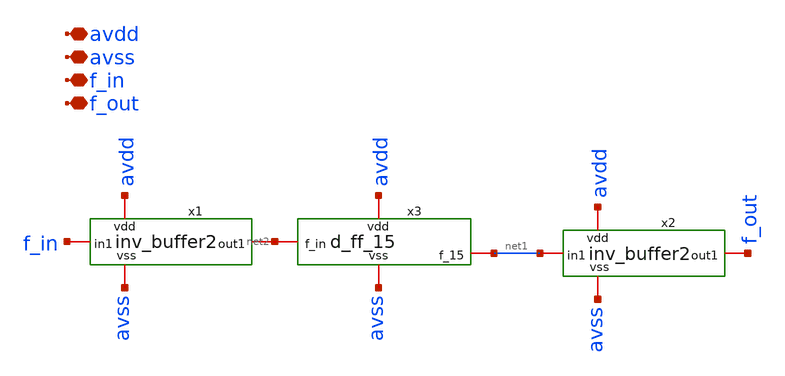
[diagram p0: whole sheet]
** sch_path: xschem/f_div.sch
**.subckt f_div avdd avss f_in f_out
*.iopin avdd
*.iopin avss
*.iopin f_in
*.iopin f_out
x1 avdd avss net2 f_in inv_buffer2
x2 avdd avss f_out net1 inv_buffer2
x3 avdd avss net2 net1 d_ff_15
**.ends

* expanding   symbol:  inv_buffer2.sym # of pins=4
** sym_path: xschem/inv_buffer2.sym
** sch_path: xschem/inv_buffer2.sch
.subckt inv_buffer2 vdd vss out1 in1
*.iopin in1
*.iopin out1
*.iopin vdd
*.iopin vss
XM4 out1 net1 vss vss sky130_fd_pr__nfet_01v8 L=0.15 W=2.8 nf=4 ad='int((nf+1)/2) * W/nf * 0.29' as='int((nf+2)/2) * W/nf * 0.29'
+ pd='2*int((nf+1)/2) * (W/nf + 0.29)' ps='2*int((nf+2)/2) * (W/nf + 0.29)' nrd='0.29 / W' nrs='0.29 / W'
+ sa=0 sb=0 sd=0 mult=1 m=1
XM1 out1 net1 vdd vdd sky130_fd_pr__pfet_01v8 L=0.15 W=5.6 nf=8 ad='int((nf+1)/2) * W/nf * 0.29' as='int((nf+2)/2) * W/nf * 0.29'
+ pd='2*int((nf+1)/2) * (W/nf + 0.29)' ps='2*int((nf+2)/2) * (W/nf + 0.29)' nrd='0.29 / W' nrs='0.29 / W'
+ sa=0 sb=0 sd=0 mult=1 m=1
XM5 vdd vdd vdd vdd sky130_fd_pr__pfet_01v8 L=0.15 W=1.4 nf=2 ad='int((nf+1)/2) * W/nf * 0.29' as='int((nf+2)/2) * W/nf * 0.29'
+ pd='2*int((nf+1)/2) * (W/nf + 0.29)' ps='2*int((nf+2)/2) * (W/nf + 0.29)' nrd='0.29 / W' nrs='0.29 / W'
+ sa=0 sb=0 sd=0 mult=1 m=1
XM6 vss vss vss vss sky130_fd_pr__nfet_01v8 L=0.15 W=1.4 nf=2 ad='int((nf+1)/2) * W/nf * 0.29' as='int((nf+2)/2) * W/nf * 0.29'
+ pd='2*int((nf+1)/2) * (W/nf + 0.29)' ps='2*int((nf+2)/2) * (W/nf + 0.29)' nrd='0.29 / W' nrs='0.29 / W'
+ sa=0 sb=0 sd=0 mult=1 m=1
x1 vdd in1 net1 vss inv_simple1
.ends


* expanding   symbol:  d_ff_15.sym # of pins=4
** sym_path: xschem/d_ff_15.sym
** sch_path: xschem/d_ff_15.sch
.subckt d_ff_15 vdd vss f_in f_15
*.iopin vdd
*.iopin vss
*.iopin f_in
*.iopin f_15
x1 f_in net3 vss vss vdd vdd f_5 q_1 sky130_fd_sc_hd__dfxbp_1
x5 net2 net1 vss vss vdd vdd net3 sky130_fd_sc_hd__nand2_1
x2 f_in f_5 vss vss vdd vdd net1 q_2 sky130_fd_sc_hd__dfxbp_1
x3 f_in net1 vss vss vdd vdd net2 q_3 sky130_fd_sc_hd__dfxbp_1
x4 f_5 net5 vss vss vdd vdd net4 q_4 sky130_fd_sc_hd__dfxbp_1
x6 f_5 net4 vss vss vdd vdd net6 f_15 sky130_fd_sc_hd__dfxbp_1
x7 net6 net4 vss vss vdd vdd net5 sky130_fd_sc_hd__nand2_1
.ends


* expanding   symbol:  inv_simple1.sym # of pins=4
** sym_path: xschem/inv_simple1.sym
** sch_path: xschem/inv_simple1.sch
.subckt inv_simple1 vdd in out vss
*.iopin in
*.iopin vdd
*.iopin vss
*.iopin out
XM19 out in vss vss sky130_fd_pr__nfet_01v8 L=0.15 W=1.4 nf=1 ad='int((nf+1)/2) * W/nf * 0.29' as='int((nf+2)/2) * W/nf * 0.29'
+ pd='2*int((nf+1)/2) * (W/nf + 0.29)' ps='2*int((nf+2)/2) * (W/nf + 0.29)' nrd='0.29 / W' nrs='0.29 / W'
+ sa=0 sb=0 sd=0 mult=1 m=1
XM20 out in vdd vdd sky130_fd_pr__pfet_01v8 L=0.15 W=2.8 nf=1 ad='int((nf+1)/2) * W/nf * 0.29' as='int((nf+2)/2) * W/nf * 0.29'
+ pd='2*int((nf+1)/2) * (W/nf + 0.29)' ps='2*int((nf+2)/2) * (W/nf + 0.29)' nrd='0.29 / W' nrs='0.29 / W'
+ sa=0 sb=0 sd=0 mult=1 m=1
XM1 vdd vdd vdd vdd sky130_fd_pr__pfet_01v8 L=0.15 W=1.4 nf=1 ad='int((nf+1)/2) * W/nf * 0.29' as='int((nf+2)/2) * W/nf * 0.29'
+ pd='2*int((nf+1)/2) * (W/nf + 0.29)' ps='2*int((nf+2)/2) * (W/nf + 0.29)' nrd='0.29 / W' nrs='0.29 / W'
+ sa=0 sb=0 sd=0 mult=1 m=1
XM2 vss vss vss vss sky130_fd_pr__nfet_01v8 L=0.15 W=1.4 nf=1 ad='int((nf+1)/2) * W/nf * 0.29' as='int((nf+2)/2) * W/nf * 0.29'
+ pd='2*int((nf+1)/2) * (W/nf + 0.29)' ps='2*int((nf+2)/2) * (W/nf + 0.29)' nrd='0.29 / W' nrs='0.29 / W'
+ sa=0 sb=0 sd=0 mult=1 m=1
.ends

.end
